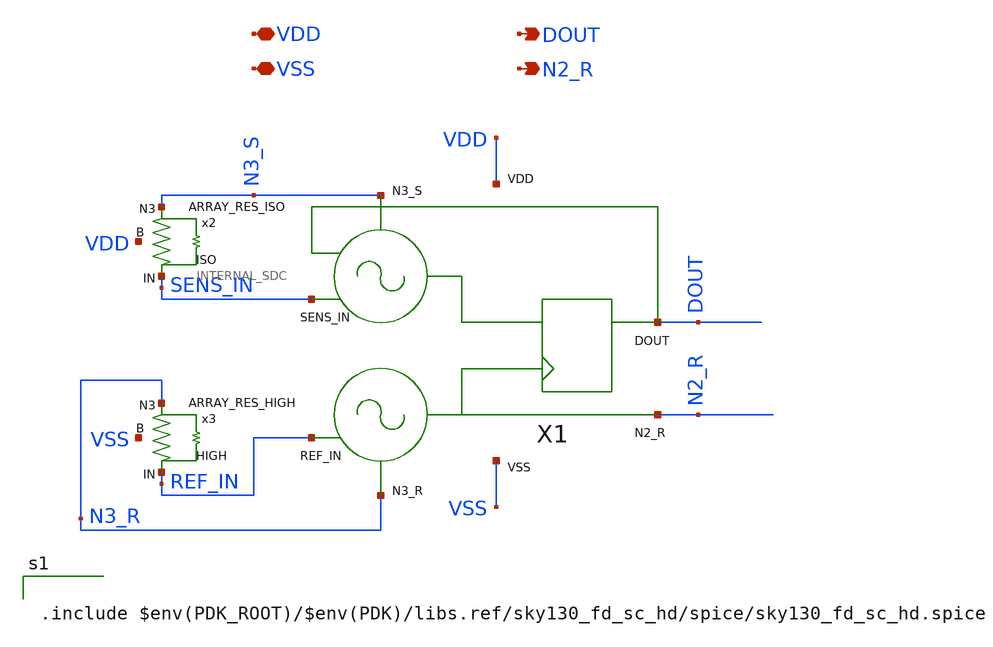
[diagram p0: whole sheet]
** sch_path: modules/SDC/symbol/SDC.sch
**.subckt SDC VDD VSS DOUT N2_R
*.iopin VDD
*.iopin VSS
*.opin DOUT
*.opin N2_R
X1 SENS_IN REF_IN DOUT VDD VSS N3_S N3_R N2_R INTERNAL_SDC
x2 N3_S SENS_IN VDD ARRAY_RES_ISO
x3 N3_R REF_IN VSS ARRAY_RES_HIGH
**** begin user architecture code

.include $env(PDK_ROOT)/$env(PDK)/libs.ref/sky130_fd_sc_hd/spice/sky130_fd_sc_hd.spice

**** end user architecture code
**.ends
.end
